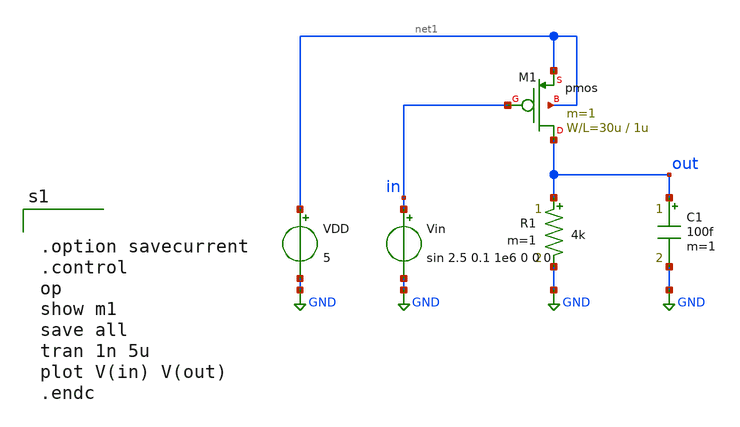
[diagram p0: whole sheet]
** sch_path: member_project/GroupWork/Team_masahiro/pfet_common_source_tran.sch
**.subckt pfet_common_source_tran
R1 out GND 4k m=1
VDD net1 GND 5
Vin in GND sin 2.5 0.1 1e6 0 0 0
M1 out in net1 net1 pmos L=1u W=30u m=1
C1 out GND 100f m=1
**** begin user architecture code
 .include $::LIB/mos.lib
.include $::LIB/passive.lib
.include $::LIB/diode.lib


.option savecurrent
.control
op
show m1
save all
tran 1n 5u
plot V(in) V(out)
.endc


**** end user architecture code
**.ends
.GLOBAL GND
.end
